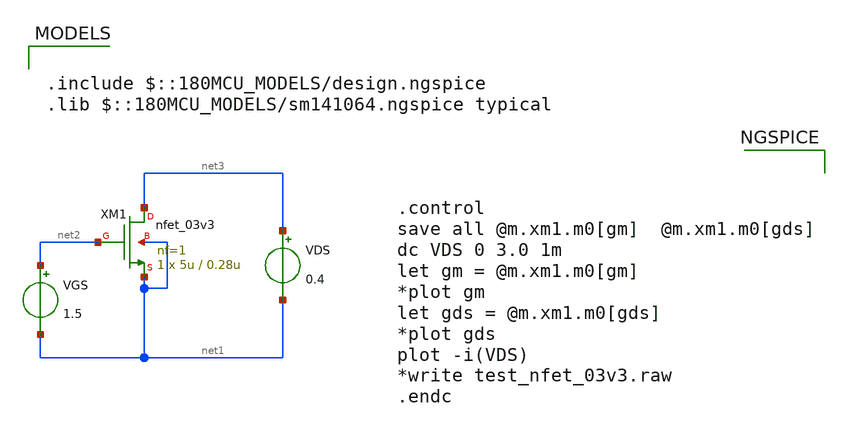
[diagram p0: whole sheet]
** sch_path: SCOP_INPUT_AND_MUX_PAKISTAN_03/Xschem/Others/nmos.sch
**.subckt nmos
XM1 net3 net2 net1 net1 nfet_03v3 L=0.28u W=5u nf=1 ad='int((nf+1)/2) * W/nf * 0.18u' as='int((nf+2)/2) * W/nf * 0.18u'
+ pd='2*int((nf+1)/2) * (W/nf + 0.18u)' ps='2*int((nf+2)/2) * (W/nf + 0.18u)' nrd='0.18u / W' nrs='0.18u / W'
+ sa=0 sb=0 sd=0 m=1
VDS net3 net1 0.4
VGS net2 net1 1.5
**** begin user architecture code



.control
save all @m.xm1.m0[gm]  @m.xm1.m0[gds]
dc VDS 0 3.0 1m
let gm = @m.xm1.m0[gm]
*plot gm
let gds = @m.xm1.m0[gds]
*plot gds
plot -i(VDS)
*write test_nfet_03v3.raw
.endc



.include $::180MCU_MODELS/design.ngspice
.lib $::180MCU_MODELS/sm141064.ngspice typical

**** end user architecture code
**.ends
.end
